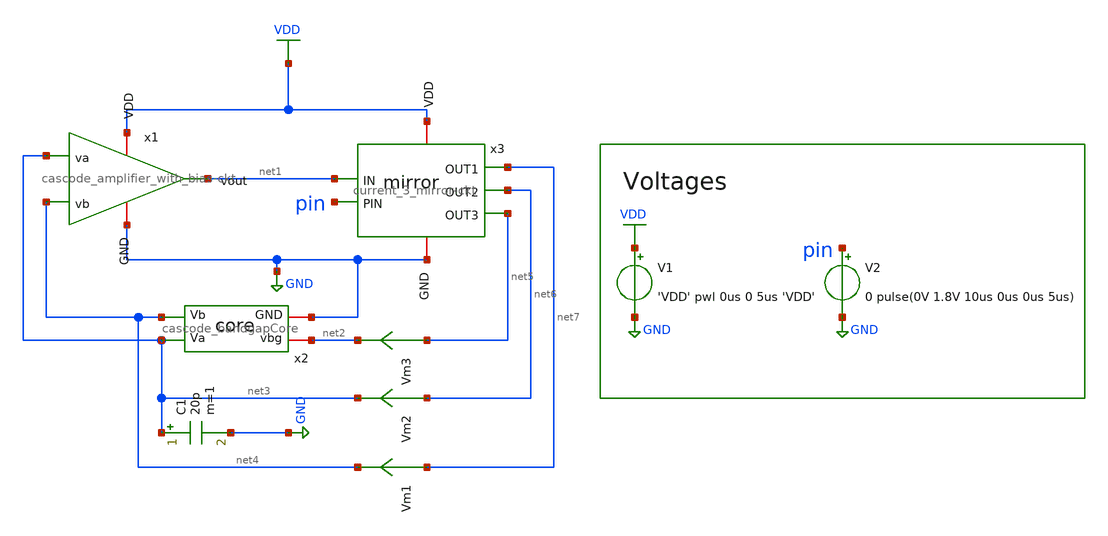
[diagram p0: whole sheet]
** sch_path: bandgap_sky130_v1/cascode_bandgap_real_op.sch
**.subckt cascode_bandgap_real_op
V1 VDD GND 'VDD' pwl 0us 0 5us 'VDD'
V2 pin GND 0 pulse(0V 1.8V 10us 0us 0us 5us)
Vm1 net7 net4 0
.save i(vm1)
Vm2 net6 net3 0
.save i(vm2)
x1 net3 net4 net1 VDD GND cascode_amplifier_with_bias-ckt
Vm3 net5 net2 0
.save i(vm3)
x3 net1 pin net7 net6 net5 VDD GND current_3_mirror-ckt
C1 net3 GND 20p m=1
x2 net3 net4 net2 GND cascode_bandgapCore
**** begin user architecture code

** opencircuitdesign pdks install
.lib $::SKYWATER_MODELS/sky130.lib.spice tt


**** end user architecture code
**.ends
.GLOBAL VDD
.GLOBAL GND
.end
